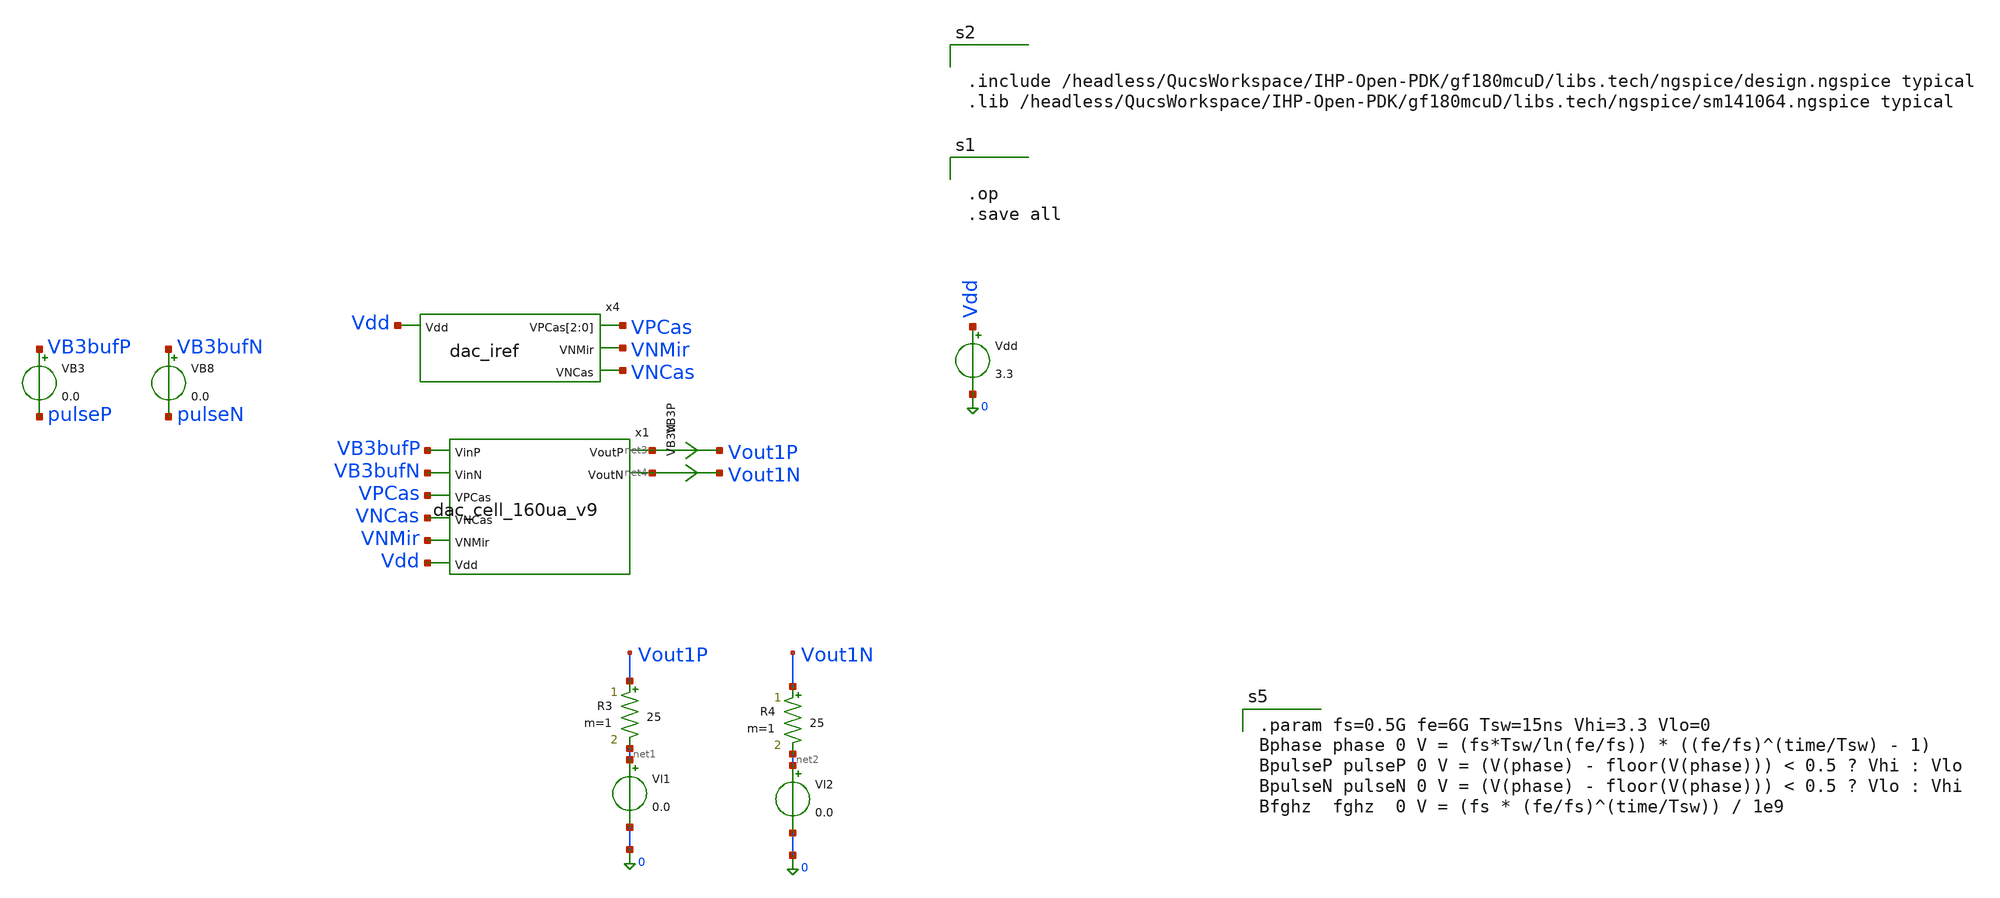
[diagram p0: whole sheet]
** sch_path: blocks/dac/test/test_dac_fsweep_160ua.sch
**.subckt test_dac_fsweep_160ua
Vdd Vdd 0 3.3
.save i(vdd)
R3 Vout1P net1 25 m=1
R4 Vout1N net2 25 m=1
Vl1 net1 0 0.0
.save i(vl1)
Vl2 net2 0 0.0
.save i(vl2)
VB3 VB3bufP pulseP 0.0
.save i(vb3)
VB8 VB3bufN pulseN 0.0
.save i(vb8)
x4 Vdd VPCas VPCas VPCas VNMir VNCas dac_iref
VB3P net3 Vout1P 0
.save i(vb3p)
VB3N net4 Vout1N 0
.save i(vb3n)
x1 net3 VB3bufP net4 VB3bufN VPCas VNCas VNMir Vdd dac_cell_160ua_v9
**** begin user architecture code



.save all
.control

tran 1p 5ns
* plot VU1syncP+6 VU1syncN+6 VU2syncP+6 VU2syncN+6 VgN+12 VgP Dm ClkP+18 ClkN+18 i(Vl1)*5E4-6
*+ i(Vl2)*5E4-6 (i(Vl1)-i(Vl2))*5E4-12
* plot ClkP+6 ClkN+6 VU0in VB1in VU0syncP-6 VU0syncN-12 VB1syncP-6 VB1syncN-12
* plot Vout1P+15E-3 Vout1N+15E-3 Vout1P-Vout1N
* plot ClkP+5 ClkN+5 VB3syncP VB3syncN VB3bufP-5 VB3bufN-5 xb3.x1.Vg1P-10 xb3.x1.Vg1N-10
plot 3.3-xb3.x1.Vg1P 3.3-xb3.x1.Vg1N

* plot x1.x1.Vcx x1.x1.Vg1P x1.x1.Vg1N

* plot VB1syncP VB1syncN-6 VB4syncN-6 VU0bufP-12 VB1bufP-12 VB4bufP-12 VU0bufN-18 VB1bufN-18
*+ VB4bufN-18
plot i(Vl1)-i(Vl2) i(Vl1)+100E-6 i(Vl2)+100E-6

let imax = 160E-6
let imin = -160E-6
plot i(VB3P)-i(VB3N) imax imin

let diff = i(Vl1)-i(Vl2)
plot pulseP diff/{imax}*5 fghz
* plot pulseP fghz

* plot i(VoutB3P)+100E-6 i(VoutB3N)+100E-6 i(VoutB3P)-i(VoutB3N) i(VoutB3N)+i(VoutB3P)
*+ i(v.x1.Vcrr1)-200E-6 i(v.x1.Vcrr2)-200E-6
* plot i(v.x1.Vcrr1) i(v.x1.Vcrr2)
* plot i(Vl1) VB1in/5E4+200E-6 VU0in/5E4+200E-6
* wrdata /foss/designs/dds/dac_isource_unary_pmos_80ua_v4_tt_500ps.csv ClkP ClkN Din VdsyncP VdsyncN
*+ i(Vl1) i(Vl2)
.endc





.op
.save all




.include /headless/QucsWorkspace/IHP-Open-PDK/gf180mcuD/libs.tech/ngspice/design.ngspice typical
.lib /headless/QucsWorkspace/IHP-Open-PDK/gf180mcuD/libs.tech/ngspice/sm141064.ngspice typical



.param fs=0.5G fe=6G Tsw=15ns Vhi=3.3 Vlo=0
Bphase phase 0 V = (fs*Tsw/ln(fe/fs)) * ((fe/fs)^(time/Tsw) - 1)
BpulseP pulseP 0 V = (V(phase) - floor(V(phase))) < 0.5 ? Vhi : Vlo
BpulseN pulseN 0 V = (V(phase) - floor(V(phase))) < 0.5 ? Vlo : Vhi
Bfghz  fghz  0 V = (fs * (fe/fs)^(time/Tsw)) / 1e9



**** end user architecture code
**.ends

* expanding   symbol:  iref/dac_iref.sym # of pins=4
** sym_path: blocks/dac/iref/dac_iref.sym
** sch_path: blocks/dac/iref/dac_iref.sch
.subckt dac_iref Vdd VPCas[2] VPCas[1] VPCas[0] VNMir VNCas
*.ipin Vdd
*.opin VPCas[2],VPCas[1],VPCas[0]
*.opin VNMir
*.opin VNCas
XM69 net3 net2 0 0 nfet_03v3 L=2u W=6u nf=1 ad='int((nf+1)/2) * W/nf * 0.18u' as='int((nf+2)/2) * W/nf * 0.18u'
+ pd='2*int((nf+1)/2) * (W/nf + 0.18u)' ps='2*int((nf+2)/2) * (W/nf + 0.18u)' nrd='0.18u / W' nrs='0.18u / W'
+ sa=0 sb=0 sd=0 m=1
XM70 net2 net1 0 0 nfet_03v3 L=2u W=4u nf=1 ad='int((nf+1)/2) * W/nf * 0.18u' as='int((nf+2)/2) * W/nf * 0.18u'
+ pd='2*int((nf+1)/2) * (W/nf + 0.18u)' ps='2*int((nf+2)/2) * (W/nf + 0.18u)' nrd='0.18u / W' nrs='0.18u / W'
+ sa=0 sb=0 sd=0 m=1
XM71 net1 net4 Vdd Vdd pfet_03v3 L=2u W=6u nf=1 ad='int((nf+1)/2) * W/nf * 0.18u' as='int((nf+2)/2) * W/nf * 0.18u'
+ pd='2*int((nf+1)/2) * (W/nf + 0.18u)' ps='2*int((nf+2)/2) * (W/nf + 0.18u)' nrd='0.18u / W' nrs='0.18u / W'
+ sa=0 sb=0 sd=0 m=1
XM72 net4 net3 Vdd Vdd pfet_03v3 L=2u W=5u nf=1 ad='int((nf+1)/2) * W/nf * 0.18u' as='int((nf+2)/2) * W/nf * 0.18u'
+ pd='2*int((nf+1)/2) * (W/nf + 0.18u)' ps='2*int((nf+2)/2) * (W/nf + 0.18u)' nrd='0.18u / W' nrs='0.18u / W'
+ sa=0 sb=0 sd=0 m=1
x1[2] Vdd VPCas[2] net4 VPCas[2] Vbias ota5t
x1[1] Vdd VPCas[1] net4 VPCas[1] Vbias ota5t
x1[0] Vdd VPCas[0] net4 VPCas[0] Vbias ota5t
XC7 net4 0 cap_mim_2f0_m3m4_noshield c_width=25e-6 c_length=20e-6 m=1
XC2[2] VPCas[2] 0 cap_mim_2f0_m3m4_noshield c_width=10e-6 c_length=5e-6 m=1
XC2[1] VPCas[1] 0 cap_mim_2f0_m3m4_noshield c_width=10e-6 c_length=5e-6 m=1
XC2[0] VPCas[0] 0 cap_mim_2f0_m3m4_noshield c_width=10e-6 c_length=5e-6 m=1
XM7 net6 net6 Vdd Vdd pfet_03v3 L=1u W=6u nf=1 ad='int((nf+1)/2) * W/nf * 0.18u' as='int((nf+2)/2) * W/nf * 0.18u'
+ pd='2*int((nf+1)/2) * (W/nf + 0.18u)' ps='2*int((nf+2)/2) * (W/nf + 0.18u)' nrd='0.18u / W' nrs='0.18u / W'
+ sa=0 sb=0 sd=0 m=1
XM8 net5 net5 net6 Vdd pfet_03v3 L=1u W=6u nf=1 ad='int((nf+1)/2) * W/nf * 0.18u' as='int((nf+2)/2) * W/nf * 0.18u'
+ pd='2*int((nf+1)/2) * (W/nf + 0.18u)' ps='2*int((nf+2)/2) * (W/nf + 0.18u)' nrd='0.18u / W' nrs='0.18u / W'
+ sa=0 sb=0 sd=0 m=1
Iref2 net5 0 DC 10uA AC 0
XM9 net7 net6 Vdd Vdd pfet_03v3 L=1u W=6u nf=1 ad='int((nf+1)/2) * W/nf * 0.18u' as='int((nf+2)/2) * W/nf * 0.18u'
+ pd='2*int((nf+1)/2) * (W/nf + 0.18u)' ps='2*int((nf+2)/2) * (W/nf + 0.18u)' nrd='0.18u / W' nrs='0.18u / W'
+ sa=0 sb=0 sd=0 m=1
XM10 VNMir net5 net7 Vdd pfet_03v3 L=1u W=6u nf=1 ad='int((nf+1)/2) * W/nf * 0.18u' as='int((nf+2)/2) * W/nf * 0.18u'
+ pd='2*int((nf+1)/2) * (W/nf + 0.18u)' ps='2*int((nf+2)/2) * (W/nf + 0.18u)' nrd='0.18u / W' nrs='0.18u / W'
+ sa=0 sb=0 sd=0 m=1
XM11 VNMir VNMir 0 0 nfet_03v3 L=4u W=2u nf=1 ad='int((nf+1)/2) * W/nf * 0.18u' as='int((nf+2)/2) * W/nf * 0.18u'
+ pd='2*int((nf+1)/2) * (W/nf + 0.18u)' ps='2*int((nf+2)/2) * (W/nf + 0.18u)' nrd='0.18u / W' nrs='0.18u / W'
+ sa=0 sb=0 sd=0 m=1
XM12 net8 net6 Vdd Vdd pfet_03v3 L=1u W=6u nf=1 ad='int((nf+1)/2) * W/nf * 0.18u' as='int((nf+2)/2) * W/nf * 0.18u'
+ pd='2*int((nf+1)/2) * (W/nf + 0.18u)' ps='2*int((nf+2)/2) * (W/nf + 0.18u)' nrd='0.18u / W' nrs='0.18u / W'
+ sa=0 sb=0 sd=0 m=1
XM14 VNCas net5 net8 Vdd pfet_03v3 L=1u W=6u nf=1 ad='int((nf+1)/2) * W/nf * 0.18u' as='int((nf+2)/2) * W/nf * 0.18u'
+ pd='2*int((nf+1)/2) * (W/nf + 0.18u)' ps='2*int((nf+2)/2) * (W/nf + 0.18u)' nrd='0.18u / W' nrs='0.18u / W'
+ sa=0 sb=0 sd=0 m=1
XM16 net9 VNCas 0 0 nfet_03v3 L=1u W=2u nf=1 ad='int((nf+1)/2) * W/nf * 0.18u' as='int((nf+2)/2) * W/nf * 0.18u'
+ pd='2*int((nf+1)/2) * (W/nf + 0.18u)' ps='2*int((nf+2)/2) * (W/nf + 0.18u)' nrd='0.18u / W' nrs='0.18u / W'
+ sa=0 sb=0 sd=0 m=1
XM17 VNCas VNMir net9 0 nfet_03v3 L=1u W=2u nf=1 ad='int((nf+1)/2) * W/nf * 0.18u' as='int((nf+2)/2) * W/nf * 0.18u'
+ pd='2*int((nf+1)/2) * (W/nf + 0.18u)' ps='2*int((nf+2)/2) * (W/nf + 0.18u)' nrd='0.18u / W' nrs='0.18u / W'
+ sa=0 sb=0 sd=0 m=1
XM4 Vbias VNMir net10 0 nfet_03v3 L=1u W=2u nf=1 ad='int((nf+1)/2) * W/nf * 0.18u' as='int((nf+2)/2) * W/nf * 0.18u'
+ pd='2*int((nf+1)/2) * (W/nf + 0.18u)' ps='2*int((nf+2)/2) * (W/nf + 0.18u)' nrd='0.18u / W' nrs='0.18u / W'
+ sa=0 sb=0 sd=0 m=1
XM5 Vbias Vbias Vdd Vdd pfet_03v3 L=1u W=4u nf=1 ad='int((nf+1)/2) * W/nf * 0.18u' as='int((nf+2)/2) * W/nf * 0.18u'
+ pd='2*int((nf+1)/2) * (W/nf + 0.18u)' ps='2*int((nf+2)/2) * (W/nf + 0.18u)' nrd='0.18u / W' nrs='0.18u / W'
+ sa=0 sb=0 sd=0 m=1
XM13 net10 VNCas 0 0 nfet_03v3 L=1u W=2u nf=1 ad='int((nf+1)/2) * W/nf * 0.18u' as='int((nf+2)/2) * W/nf * 0.18u'
+ pd='2*int((nf+1)/2) * (W/nf + 0.18u)' ps='2*int((nf+2)/2) * (W/nf + 0.18u)' nrd='0.18u / W' nrs='0.18u / W'
+ sa=0 sb=0 sd=0 m=1
XR3 net4 net3 Vdd ppolyf_u_1k r_width=1e-6 r_length=4e-6 m=1
XR2 net1 net2 Vdd ppolyf_u_1k r_width=1e-6 r_length=8e-6 m=1
.ends


* expanding   symbol:  cellv9/dac_cell_160ua_v9.sym # of pins=8
** sym_path: blocks/dac/cellv9/dac_cell_160ua_v9.sym
** sch_path: blocks/dac/cellv9/dac_cell_160ua_v9.sch
.subckt dac_cell_160ua_v9 VoutP VinP VoutN VinN VPCas VNCas VNMir Vdd
*.opin VoutP
*.opin VoutN
*.ipin VinP
*.ipin VinN
*.ipin Vdd
*.ipin VPCas
*.ipin VNCas
*.ipin VNMir
x5 VoutP VinP VoutN VinN VPCas VNCas VNMir Vdd dac_cell_80ua_v9
x2 VoutP VinP VoutN VinN VPCas VNCas VNMir Vdd dac_cell_80ua_v9
.ends


* expanding   symbol:  common/ota5t.sym # of pins=5
** sym_path: blocks/dac/common/ota5t.sym
** sch_path: blocks/dac/common/ota5t.sch
.subckt ota5t Vdd VinN VinP Vout Vbias
*.ipin VinP
*.ipin VinN
*.opin Vout
*.ipin Vdd
*.ipin Vbias
XM16 Vout net2 0 0 nfet_03v3 L=1u W=2u nf=1 ad='int((nf+1)/2) * W/nf * 0.18u' as='int((nf+2)/2) * W/nf * 0.18u'
+ pd='2*int((nf+1)/2) * (W/nf + 0.18u)' ps='2*int((nf+2)/2) * (W/nf + 0.18u)' nrd='0.18u / W' nrs='0.18u / W'
+ sa=0 sb=0 sd=0 m=1
XM1 Vout VinN net1 Vdd pfet_03v3 L=1u W=4u nf=1 ad='int((nf+1)/2) * W/nf * 0.18u' as='int((nf+2)/2) * W/nf * 0.18u'
+ pd='2*int((nf+1)/2) * (W/nf + 0.18u)' ps='2*int((nf+2)/2) * (W/nf + 0.18u)' nrd='0.18u / W' nrs='0.18u / W'
+ sa=0 sb=0 sd=0 m=1
XM19 net2 VinP net1 Vdd pfet_03v3 L=1u W=4u nf=1 ad='int((nf+1)/2) * W/nf * 0.18u' as='int((nf+2)/2) * W/nf * 0.18u'
+ pd='2*int((nf+1)/2) * (W/nf + 0.18u)' ps='2*int((nf+2)/2) * (W/nf + 0.18u)' nrd='0.18u / W' nrs='0.18u / W'
+ sa=0 sb=0 sd=0 m=1
XM22 net2 net2 0 0 nfet_03v3 L=1u W=2u nf=1 ad='int((nf+1)/2) * W/nf * 0.18u' as='int((nf+2)/2) * W/nf * 0.18u'
+ pd='2*int((nf+1)/2) * (W/nf + 0.18u)' ps='2*int((nf+2)/2) * (W/nf + 0.18u)' nrd='0.18u / W' nrs='0.18u / W'
+ sa=0 sb=0 sd=0 m=1
.param bbW=2u
.param bbL=1u
XM29 net1 Vbias Vdd Vdd pfet_03v3 L=1u W=4u nf=1 ad='int((nf+1)/2) * W/nf * 0.18u' as='int((nf+2)/2) * W/nf * 0.18u'
+ pd='2*int((nf+1)/2) * (W/nf + 0.18u)' ps='2*int((nf+2)/2) * (W/nf + 0.18u)' nrd='0.18u / W' nrs='0.18u / W'
+ sa=0 sb=0 sd=0 m=2
.ends


* expanding   symbol:  cellv9/dac_cell_80ua_v9.sym # of pins=8
** sym_path: blocks/dac/cellv9/dac_cell_80ua_v9.sym
** sch_path: blocks/dac/cellv9/dac_cell_80ua_v9.sch
.subckt dac_cell_80ua_v9 VoutP VinP VoutN VinN VPCas VNCas VNMir Vdd
*.opin VoutP
*.opin VoutN
*.ipin VinP
*.ipin VinN
*.ipin Vdd
*.ipin VPCas
*.ipin VNCas
*.ipin VNMir
.param cmLw=0.4u
.param cmHw=0.7u
.param cmLfbw=1.0u
.param cmHfbw=0.22u
XM20 VxP Vg1P Vcx Vdd pfet_03v3 L=0.28u W={cswW} nf=1 ad='int((nf+1)/2) * W/nf * 0.18u' as='int((nf+2)/2) * W/nf * 0.18u'
+ pd='2*int((nf+1)/2) * (W/nf + 0.18u)' ps='2*int((nf+2)/2) * (W/nf + 0.18u)' nrd='0.18u / W' nrs='0.18u / W'
+ sa=0 sb=0 sd=0 m=1
XM21 VxN Vg1N Vcx Vdd pfet_03v3 L=0.28u W={cswW} nf=1 ad='int((nf+1)/2) * W/nf * 0.18u' as='int((nf+2)/2) * W/nf * 0.18u'
+ pd='2*int((nf+1)/2) * (W/nf + 0.18u)' ps='2*int((nf+2)/2) * (W/nf + 0.18u)' nrd='0.18u / W' nrs='0.18u / W'
+ sa=0 sb=0 sd=0 m=1
XM22 VoutP VcbP VxP Vdd pfet_03v3 L=0.28u W={cbufW} nf=1 ad='int((nf+1)/2) * W/nf * 0.18u' as='int((nf+2)/2) * W/nf * 0.18u'
+ pd='2*int((nf+1)/2) * (W/nf + 0.18u)' ps='2*int((nf+2)/2) * (W/nf + 0.18u)' nrd='0.18u / W' nrs='0.18u / W'
+ sa=0 sb=0 sd=0 m=1
XM23 VoutN VcbN VxN Vdd pfet_03v3 L=0.28u W={cbufW} nf=1 ad='int((nf+1)/2) * W/nf * 0.18u' as='int((nf+2)/2) * W/nf * 0.18u'
+ pd='2*int((nf+1)/2) * (W/nf + 0.18u)' ps='2*int((nf+2)/2) * (W/nf + 0.18u)' nrd='0.18u / W' nrs='0.18u / W'
+ sa=0 sb=0 sd=0 m=1
XM24 net1 Vg1N Vdd Vdd pfet_03v3 L=0.28u W={invPw} nf=1 ad='int((nf+1)/2) * W/nf * 0.18u' as='int((nf+2)/2) * W/nf * 0.18u'
+ pd='2*int((nf+1)/2) * (W/nf + 0.18u)' ps='2*int((nf+2)/2) * (W/nf + 0.18u)' nrd='0.18u / W' nrs='0.18u / W'
+ sa=0 sb=0 sd=0 m=1
XM34 net1 Vg1N 0 0 nfet_03v3 L=0.28u W=0.22u nf=1 ad='int((nf+1)/2) * W/nf * 0.18u' as='int((nf+2)/2) * W/nf * 0.18u'
+ pd='2*int((nf+1)/2) * (W/nf + 0.18u)' ps='2*int((nf+2)/2) * (W/nf + 0.18u)' nrd='0.18u / W' nrs='0.18u / W'
+ sa=0 sb=0 sd=0 m=1
XM35 VoutN net1 VoutN Vdd pfet_03v3 L=0.28u W={dummyW} nf=1 ad='int((nf+1)/2) * W/nf * 0.18u' as='int((nf+2)/2) * W/nf * 0.18u'
+ pd='2*int((nf+1)/2) * (W/nf + 0.18u)' ps='2*int((nf+2)/2) * (W/nf + 0.18u)' nrd='0.18u / W' nrs='0.18u / W'
+ sa=0 sb=0 sd=0 m=1
XM36 net2 Vg1P Vdd Vdd pfet_03v3 L=0.28u W={invPw} nf=1 ad='int((nf+1)/2) * W/nf * 0.18u' as='int((nf+2)/2) * W/nf * 0.18u'
+ pd='2*int((nf+1)/2) * (W/nf + 0.18u)' ps='2*int((nf+2)/2) * (W/nf + 0.18u)' nrd='0.18u / W' nrs='0.18u / W'
+ sa=0 sb=0 sd=0 m=1
XM37 net2 Vg1P 0 0 nfet_03v3 L=0.28u W=0.22u nf=1 ad='int((nf+1)/2) * W/nf * 0.18u' as='int((nf+2)/2) * W/nf * 0.18u'
+ pd='2*int((nf+1)/2) * (W/nf + 0.18u)' ps='2*int((nf+2)/2) * (W/nf + 0.18u)' nrd='0.18u / W' nrs='0.18u / W'
+ sa=0 sb=0 sd=0 m=1
XM38 VoutP net2 VoutP Vdd pfet_03v3 L=0.28u W={dummyW} nf=1 ad='int((nf+1)/2) * W/nf * 0.18u' as='int((nf+2)/2) * W/nf * 0.18u'
+ pd='2*int((nf+1)/2) * (W/nf + 0.18u)' ps='2*int((nf+2)/2) * (W/nf + 0.18u)' nrd='0.18u / W' nrs='0.18u / W'
+ sa=0 sb=0 sd=0 m=1
VcbRef3 VcbRef 0 {Vcbias}
.save i(vcbref3)
.param VcBias=0.84
.param casW=4u
XM39 net3 VinPDr VH Vdd pfet_03v3 L=0.28u W={cmHw} nf=1 ad='int((nf+1)/2) * W/nf * 0.18u' as='int((nf+2)/2) * W/nf * 0.18u'
+ pd='2*int((nf+1)/2) * (W/nf + 0.18u)' ps='2*int((nf+2)/2) * (W/nf + 0.18u)' nrd='0.18u / W' nrs='0.18u / W'
+ sa=0 sb=0 sd=0 m=1
XM40 Vg1P VinPDr net3 Vdd pfet_03v3 L=0.28u W={cmHw} nf=1 ad='int((nf+1)/2) * W/nf * 0.18u' as='int((nf+2)/2) * W/nf * 0.18u'
+ pd='2*int((nf+1)/2) * (W/nf + 0.18u)' ps='2*int((nf+2)/2) * (W/nf + 0.18u)' nrd='0.18u / W' nrs='0.18u / W'
+ sa=0 sb=0 sd=0 m=1
XM41 Vg1P VinPDr VL 0 nfet_03v3 L=0.28u W={cmLw} nf=1 ad='int((nf+1)/2) * W/nf * 0.18u' as='int((nf+2)/2) * W/nf * 0.18u'
+ pd='2*int((nf+1)/2) * (W/nf + 0.18u)' ps='2*int((nf+2)/2) * (W/nf + 0.18u)' nrd='0.18u / W' nrs='0.18u / W'
+ sa=0 sb=0 sd=0 m=1
XM42 net3 VinNDr VH Vdd pfet_03v3 L=0.28u W={cmHfbW} nf=1 ad='int((nf+1)/2) * W/nf * 0.18u' as='int((nf+2)/2) * W/nf * 0.18u'
+ pd='2*int((nf+1)/2) * (W/nf + 0.18u)' ps='2*int((nf+2)/2) * (W/nf + 0.18u)' nrd='0.18u / W' nrs='0.18u / W'
+ sa=0 sb=0 sd=0 m=1
XM43 net4 VinNDr VH Vdd pfet_03v3 L=0.28u W={cmHw} nf=1 ad='int((nf+1)/2) * W/nf * 0.18u' as='int((nf+2)/2) * W/nf * 0.18u'
+ pd='2*int((nf+1)/2) * (W/nf + 0.18u)' ps='2*int((nf+2)/2) * (W/nf + 0.18u)' nrd='0.18u / W' nrs='0.18u / W'
+ sa=0 sb=0 sd=0 m=1
XM44 Vg1N VinNDr net4 Vdd pfet_03v3 L=0.28u W={cmHw} nf=1 ad='int((nf+1)/2) * W/nf * 0.18u' as='int((nf+2)/2) * W/nf * 0.18u'
+ pd='2*int((nf+1)/2) * (W/nf + 0.18u)' ps='2*int((nf+2)/2) * (W/nf + 0.18u)' nrd='0.18u / W' nrs='0.18u / W'
+ sa=0 sb=0 sd=0 m=1
XM45 Vg1N VinNDr VL 0 nfet_03v3 L=0.28u W={cmLw} nf=1 ad='int((nf+1)/2) * W/nf * 0.18u' as='int((nf+2)/2) * W/nf * 0.18u'
+ pd='2*int((nf+1)/2) * (W/nf + 0.18u)' ps='2*int((nf+2)/2) * (W/nf + 0.18u)' nrd='0.18u / W' nrs='0.18u / W'
+ sa=0 sb=0 sd=0 m=1
XM46 net4 VinPDr VH Vdd pfet_03v3 L=0.28u W={cmHfbW} nf=1 ad='int((nf+1)/2) * W/nf * 0.18u' as='int((nf+2)/2) * W/nf * 0.18u'
+ pd='2*int((nf+1)/2) * (W/nf + 0.18u)' ps='2*int((nf+2)/2) * (W/nf + 0.18u)' nrd='0.18u / W' nrs='0.18u / W'
+ sa=0 sb=0 sd=0 m=1
XM47 VL VinPDr Vg1N Vdd pfet_03v3 L=0.28u W={cmLfbw} nf=1 ad='int((nf+1)/2) * W/nf * 0.18u' as='int((nf+2)/2) * W/nf * 0.18u'
+ pd='2*int((nf+1)/2) * (W/nf + 0.18u)' ps='2*int((nf+2)/2) * (W/nf + 0.18u)' nrd='0.18u / W' nrs='0.18u / W'
+ sa=0 sb=0 sd=0 m=1
XM48 VL VinNDr Vg1P Vdd pfet_03v3 L=0.28u W={cmLfbw} nf=1 ad='int((nf+1)/2) * W/nf * 0.18u' as='int((nf+2)/2) * W/nf * 0.18u'
+ pd='2*int((nf+1)/2) * (W/nf + 0.18u)' ps='2*int((nf+2)/2) * (W/nf + 0.18u)' nrd='0.18u / W' nrs='0.18u / W'
+ sa=0 sb=0 sd=0 m=1
.param dummyW=1.0u
.param invPW=0.5u
.param cswW=3.0u
.param cbufW=3.2u
x1 VH Vdd VL clamp
.param mirW=4u
.param mirL=1u
.param casL=1u
XM4 net5 VPCas Vdd Vdd pfet_03v3 L={casL} W={casW} nf=1 ad='int((nf+1)/2) * W/nf * 0.18u' as='int((nf+2)/2) * W/nf * 0.18u'
+ pd='2*int((nf+1)/2) * (W/nf + 0.18u)' ps='2*int((nf+2)/2) * (W/nf + 0.18u)' nrd='0.18u / W' nrs='0.18u / W'
+ sa=0 sb=0 sd=0 m=1
XM7 Vcx VPMir net5 Vdd pfet_03v3 L={mirL} W={mirW} nf=1 ad='int((nf+1)/2) * W/nf * 0.18u' as='int((nf+2)/2) * W/nf * 0.18u'
+ pd='2*int((nf+1)/2) * (W/nf + 0.18u)' ps='2*int((nf+2)/2) * (W/nf + 0.18u)' nrd='0.18u / W' nrs='0.18u / W'
+ sa=0 sb=0 sd=0 m=1
XM9 net6 VPCas Vdd Vdd pfet_03v3 L={casL} W={casW} nf=1 ad='int((nf+1)/2) * W/nf * 0.18u' as='int((nf+2)/2) * W/nf * 0.18u'
+ pd='2*int((nf+1)/2) * (W/nf + 0.18u)' ps='2*int((nf+2)/2) * (W/nf + 0.18u)' nrd='0.18u / W' nrs='0.18u / W'
+ sa=0 sb=0 sd=0 m=1
XM10 Vcx VPMir net6 Vdd pfet_03v3 L={mirL} W={mirW} nf=1 ad='int((nf+1)/2) * W/nf * 0.18u' as='int((nf+2)/2) * W/nf * 0.18u'
+ pd='2*int((nf+1)/2) * (W/nf + 0.18u)' ps='2*int((nf+2)/2) * (W/nf + 0.18u)' nrd='0.18u / W' nrs='0.18u / W'
+ sa=0 sb=0 sd=0 m=1
XM11 net7 VPCas Vdd Vdd pfet_03v3 L={casL} W={casW} nf=1 ad='int((nf+1)/2) * W/nf * 0.18u' as='int((nf+2)/2) * W/nf * 0.18u'
+ pd='2*int((nf+1)/2) * (W/nf + 0.18u)' ps='2*int((nf+2)/2) * (W/nf + 0.18u)' nrd='0.18u / W' nrs='0.18u / W'
+ sa=0 sb=0 sd=0 m=1
XM12 Vcx VPMir net7 Vdd pfet_03v3 L={mirL} W={mirW} nf=1 ad='int((nf+1)/2) * W/nf * 0.18u' as='int((nf+2)/2) * W/nf * 0.18u'
+ pd='2*int((nf+1)/2) * (W/nf + 0.18u)' ps='2*int((nf+2)/2) * (W/nf + 0.18u)' nrd='0.18u / W' nrs='0.18u / W'
+ sa=0 sb=0 sd=0 m=1
XM13 net8 VPCas Vdd Vdd pfet_03v3 L={casL} W={casW} nf=1 ad='int((nf+1)/2) * W/nf * 0.18u' as='int((nf+2)/2) * W/nf * 0.18u'
+ pd='2*int((nf+1)/2) * (W/nf + 0.18u)' ps='2*int((nf+2)/2) * (W/nf + 0.18u)' nrd='0.18u / W' nrs='0.18u / W'
+ sa=0 sb=0 sd=0 m=1
XM14 Vcx VPMir net8 Vdd pfet_03v3 L={mirL} W={mirW} nf=1 ad='int((nf+1)/2) * W/nf * 0.18u' as='int((nf+2)/2) * W/nf * 0.18u'
+ pd='2*int((nf+1)/2) * (W/nf + 0.18u)' ps='2*int((nf+2)/2) * (W/nf + 0.18u)' nrd='0.18u / W' nrs='0.18u / W'
+ sa=0 sb=0 sd=0 m=1
XM1 net9 VPCas Vdd Vdd pfet_03v3 L={casL} W={casW} nf=1 ad='int((nf+1)/2) * W/nf * 0.18u' as='int((nf+2)/2) * W/nf * 0.18u'
+ pd='2*int((nf+1)/2) * (W/nf + 0.18u)' ps='2*int((nf+2)/2) * (W/nf + 0.18u)' nrd='0.18u / W' nrs='0.18u / W'
+ sa=0 sb=0 sd=0 m=1
XM5 Vcx VPMir net9 Vdd pfet_03v3 L={mirL} W={mirW} nf=1 ad='int((nf+1)/2) * W/nf * 0.18u' as='int((nf+2)/2) * W/nf * 0.18u'
+ pd='2*int((nf+1)/2) * (W/nf + 0.18u)' ps='2*int((nf+2)/2) * (W/nf + 0.18u)' nrd='0.18u / W' nrs='0.18u / W'
+ sa=0 sb=0 sd=0 m=1
XM6 net10 VPCas Vdd Vdd pfet_03v3 L={casL} W={casW} nf=1 ad='int((nf+1)/2) * W/nf * 0.18u' as='int((nf+2)/2) * W/nf * 0.18u'
+ pd='2*int((nf+1)/2) * (W/nf + 0.18u)' ps='2*int((nf+2)/2) * (W/nf + 0.18u)' nrd='0.18u / W' nrs='0.18u / W'
+ sa=0 sb=0 sd=0 m=1
XM8 Vcx VPMir net10 Vdd pfet_03v3 L={mirL} W={mirW} nf=1 ad='int((nf+1)/2) * W/nf * 0.18u' as='int((nf+2)/2) * W/nf * 0.18u'
+ pd='2*int((nf+1)/2) * (W/nf + 0.18u)' ps='2*int((nf+2)/2) * (W/nf + 0.18u)' nrd='0.18u / W' nrs='0.18u / W'
+ sa=0 sb=0 sd=0 m=1
XM15 net11 VPCas Vdd Vdd pfet_03v3 L={casL} W={casW} nf=1 ad='int((nf+1)/2) * W/nf * 0.18u' as='int((nf+2)/2) * W/nf * 0.18u'
+ pd='2*int((nf+1)/2) * (W/nf + 0.18u)' ps='2*int((nf+2)/2) * (W/nf + 0.18u)' nrd='0.18u / W' nrs='0.18u / W'
+ sa=0 sb=0 sd=0 m=1
XM16 Vcx VPMir net11 Vdd pfet_03v3 L={mirL} W={mirW} nf=1 ad='int((nf+1)/2) * W/nf * 0.18u' as='int((nf+2)/2) * W/nf * 0.18u'
+ pd='2*int((nf+1)/2) * (W/nf + 0.18u)' ps='2*int((nf+2)/2) * (W/nf + 0.18u)' nrd='0.18u / W' nrs='0.18u / W'
+ sa=0 sb=0 sd=0 m=1
XM17 net12 VPCas Vdd Vdd pfet_03v3 L={casL} W={casW} nf=1 ad='int((nf+1)/2) * W/nf * 0.18u' as='int((nf+2)/2) * W/nf * 0.18u'
+ pd='2*int((nf+1)/2) * (W/nf + 0.18u)' ps='2*int((nf+2)/2) * (W/nf + 0.18u)' nrd='0.18u / W' nrs='0.18u / W'
+ sa=0 sb=0 sd=0 m=1
XM18 Vcx VPMir net12 Vdd pfet_03v3 L={mirL} W={mirW} nf=1 ad='int((nf+1)/2) * W/nf * 0.18u' as='int((nf+2)/2) * W/nf * 0.18u'
+ pd='2*int((nf+1)/2) * (W/nf + 0.18u)' ps='2*int((nf+2)/2) * (W/nf + 0.18u)' nrd='0.18u / W' nrs='0.18u / W'
+ sa=0 sb=0 sd=0 m=1
XM2 VPMir VNMir net13 0 nfet_03v3 L=1u W=2u nf=1 ad='int((nf+1)/2) * W/nf * 0.18u' as='int((nf+2)/2) * W/nf * 0.18u'
+ pd='2*int((nf+1)/2) * (W/nf + 0.18u)' ps='2*int((nf+2)/2) * (W/nf + 0.18u)' nrd='0.18u / W' nrs='0.18u / W'
+ sa=0 sb=0 sd=0 m=1
XM3 VPMir VPMir net14 Vdd pfet_03v3 L={mirL} W={mirW} nf=1 ad='int((nf+1)/2) * W/nf * 0.18u' as='int((nf+2)/2) * W/nf * 0.18u'
+ pd='2*int((nf+1)/2) * (W/nf + 0.18u)' ps='2*int((nf+2)/2) * (W/nf + 0.18u)' nrd='0.18u / W' nrs='0.18u / W'
+ sa=0 sb=0 sd=0 m=1
XM19 net13 VNCas 0 0 nfet_03v3 L=1u W=2u nf=1 ad='int((nf+1)/2) * W/nf * 0.18u' as='int((nf+2)/2) * W/nf * 0.18u'
+ pd='2*int((nf+1)/2) * (W/nf + 0.18u)' ps='2*int((nf+2)/2) * (W/nf + 0.18u)' nrd='0.18u / W' nrs='0.18u / W'
+ sa=0 sb=0 sd=0 m=1
XM25 net14 VPCas Vdd Vdd pfet_03v3 L={casL} W={casW} nf=1 ad='int((nf+1)/2) * W/nf * 0.18u' as='int((nf+2)/2) * W/nf * 0.18u'
+ pd='2*int((nf+1)/2) * (W/nf + 0.18u)' ps='2*int((nf+2)/2) * (W/nf + 0.18u)' nrd='0.18u / W' nrs='0.18u / W'
+ sa=0 sb=0 sd=0 m=1
x2 Vdd VcbP VcbRef VcbP IB10 ota5_ab_buf_v1
x3 Vdd VcbN VcbRef VcbN IB10 ota5_ab_buf_v1
VinN net17 net18 0
.save i(vinn)
x5 net17 VinN Vdd cmos_buf
VinP net19 net20 0
.save i(vinp)
x4 net19 VinP Vdd cmos_buf
XM26 net15 VNMir net16 0 nfet_03v3 L=1u W=2u nf=1 ad='int((nf+1)/2) * W/nf * 0.18u' as='int((nf+2)/2) * W/nf * 0.18u'
+ pd='2*int((nf+1)/2) * (W/nf + 0.18u)' ps='2*int((nf+2)/2) * (W/nf + 0.18u)' nrd='0.18u / W' nrs='0.18u / W'
+ sa=0 sb=0 sd=0 m=1
XM27 net16 VNCas 0 0 nfet_03v3 L=1u W=2u nf=1 ad='int((nf+1)/2) * W/nf * 0.18u' as='int((nf+2)/2) * W/nf * 0.18u'
+ pd='2*int((nf+1)/2) * (W/nf + 0.18u)' ps='2*int((nf+2)/2) * (W/nf + 0.18u)' nrd='0.18u / W' nrs='0.18u / W'
+ sa=0 sb=0 sd=0 m=1
XM28 net15 net15 Vdd Vdd pfet_03v3 L=1u W=8u nf=1 ad='int((nf+1)/2) * W/nf * 0.18u' as='int((nf+2)/2) * W/nf * 0.18u'
+ pd='2*int((nf+1)/2) * (W/nf + 0.18u)' ps='2*int((nf+2)/2) * (W/nf + 0.18u)' nrd='0.18u / W' nrs='0.18u / W'
+ sa=0 sb=0 sd=0 m=1
XM29 IB10 net15 Vdd Vdd pfet_03v3 L=1u W=8u nf=1 ad='int((nf+1)/2) * W/nf * 0.18u' as='int((nf+2)/2) * W/nf * 0.18u'
+ pd='2*int((nf+1)/2) * (W/nf + 0.18u)' ps='2*int((nf+2)/2) * (W/nf + 0.18u)' nrd='0.18u / W' nrs='0.18u / W'
+ sa=0 sb=0 sd=0 m=1
XM30 IB10 IB10 0 0 nfet_03v3 L=1u W=8u nf=1 ad='int((nf+1)/2) * W/nf * 0.18u' as='int((nf+2)/2) * W/nf * 0.18u'
+ pd='2*int((nf+1)/2) * (W/nf + 0.18u)' ps='2*int((nf+2)/2) * (W/nf + 0.18u)' nrd='0.18u / W' nrs='0.18u / W'
+ sa=0 sb=0 sd=0 m=1
XR3 net18 VinNDr Vdd ppolyf_u_1k r_width=1e-6 r_length=1e-6 m=1
XR2 VinPDr net20 Vdd ppolyf_u_1k r_width=1e-6 r_length=1e-6 m=1
XC4 VPMir 0 cap_mim_2f0_m3m4_noshield c_width=25e-6 c_length=20e-6 m=1
XC2 IB10 0 cap_mim_2f0_m3m4_noshield c_width=25e-6 c_length=20e-6 m=1
XC7 Vdd 0 cap_mim_2f0_m3m4_noshield c_width=25e-6 c_length=20e-6 m=1
.ends


* expanding   symbol:  cellv9/clamp.sym # of pins=3
** sym_path: blocks/dac/cellv9/clamp.sym
** sch_path: blocks/dac/cellv9/clamp.sch
.subckt clamp VH Vdd VL
*.opin VH
*.opin VL
*.ipin Vdd
XM49 VL FB 0 0 nfet_03v3 L=0.28u W=2u nf=1 ad='int((nf+1)/2) * W/nf * 0.18u' as='int((nf+2)/2) * W/nf * 0.18u'
+ pd='2*int((nf+1)/2) * (W/nf + 0.18u)' ps='2*int((nf+2)/2) * (W/nf + 0.18u)' nrd='0.18u / W' nrs='0.18u / W'
+ sa=0 sb=0 sd=0 m=1
XM50 VH FB Vdd Vdd pfet_03v3 L=0.28u W=4u nf=1 ad='int((nf+1)/2) * W/nf * 0.18u' as='int((nf+2)/2) * W/nf * 0.18u'
+ pd='2*int((nf+1)/2) * (W/nf + 0.18u)' ps='2*int((nf+2)/2) * (W/nf + 0.18u)' nrd='0.18u / W' nrs='0.18u / W'
+ sa=0 sb=0 sd=0 m=1
XR3 VL FB Vdd ppolyf_u_1k r_width=1e-6 r_length=1e-6 m=1
XR1 FB VH Vdd ppolyf_u_1k r_width=1e-6 r_length=15e-6 m=1
XC2 Vdd VH cap_mim_2f0_m3m4_noshield c_width=25e-6 c_length=20e-6 m=1
XC1 Vdd VH cap_mim_2f0_m3m4_noshield c_width=10e-6 c_length=5e-6 m=1
XC3 Vdd VH cap_mim_2f0_m3m4_noshield c_width=5e-6 c_length=5e-6 m=1
XC4 VL 0 cap_mim_2f0_m3m4_noshield c_width=25e-6 c_length=20e-6 m=1
XC5 VL 0 cap_mim_2f0_m3m4_noshield c_width=10e-6 c_length=5e-6 m=1
XC6 VL 0 cap_mim_2f0_m3m4_noshield c_width=5e-6 c_length=5e-6 m=1
XC7 Vdd 0 cap_mim_2f0_m3m4_noshield c_width=25e-6 c_length=20e-6 m=1
.ends


* expanding   symbol:  cellv9/ota5_ab_buf_v1.sym # of pins=5
** sym_path: blocks/dac/cellv9/ota5_ab_buf_v1.sym
** sch_path: blocks/dac/cellv9/ota5_ab_buf_v1.sch
.subckt ota5_ab_buf_v1 Vdd VinN VinP Vout IB10
*.opin Vout
*.ipin VinP
*.ipin VinN
*.ipin Vdd
*.ipin IB10
XM16 VoOTA net2 0 0 nfet_03v3 L=1u W=10u nf=1 ad='int((nf+1)/2) * W/nf * 0.18u' as='int((nf+2)/2) * W/nf * 0.18u'
+ pd='2*int((nf+1)/2) * (W/nf + 0.18u)' ps='2*int((nf+2)/2) * (W/nf + 0.18u)' nrd='0.18u / W' nrs='0.18u / W'
+ sa=0 sb=0 sd=0 m=1
XM18 VoOTA VinN net1 Vdd pfet_03v3 L=1u W=20u nf=1 ad='int((nf+1)/2) * W/nf * 0.18u' as='int((nf+2)/2) * W/nf * 0.18u'
+ pd='2*int((nf+1)/2) * (W/nf + 0.18u)' ps='2*int((nf+2)/2) * (W/nf + 0.18u)' nrd='0.18u / W' nrs='0.18u / W'
+ sa=0 sb=0 sd=0 m=1
XM19 net2 VinP net1 Vdd pfet_03v3 L=1u W=20u nf=1 ad='int((nf+1)/2) * W/nf * 0.18u' as='int((nf+2)/2) * W/nf * 0.18u'
+ pd='2*int((nf+1)/2) * (W/nf + 0.18u)' ps='2*int((nf+2)/2) * (W/nf + 0.18u)' nrd='0.18u / W' nrs='0.18u / W'
+ sa=0 sb=0 sd=0 m=1
XM22 net2 net2 0 0 nfet_03v3 L=1u W=10u nf=1 ad='int((nf+1)/2) * W/nf * 0.18u' as='int((nf+2)/2) * W/nf * 0.18u'
+ pd='2*int((nf+1)/2) * (W/nf + 0.18u)' ps='2*int((nf+2)/2) * (W/nf + 0.18u)' nrd='0.18u / W' nrs='0.18u / W'
+ sa=0 sb=0 sd=0 m=1
XM1 net1 net3 Vdd Vdd pfet_03v3 L=1u W=40u nf=1 ad='int((nf+1)/2) * W/nf * 0.18u' as='int((nf+2)/2) * W/nf * 0.18u'
+ pd='2*int((nf+1)/2) * (W/nf + 0.18u)' ps='2*int((nf+2)/2) * (W/nf + 0.18u)' nrd='0.18u / W' nrs='0.18u / W'
+ sa=0 sb=0 sd=0 m=1
XM2 net3 net3 Vdd Vdd pfet_03v3 L=1u W=40u nf=1 ad='int((nf+1)/2) * W/nf * 0.18u' as='int((nf+2)/2) * W/nf * 0.18u'
+ pd='2*int((nf+1)/2) * (W/nf + 0.18u)' ps='2*int((nf+2)/2) * (W/nf + 0.18u)' nrd='0.18u / W' nrs='0.18u / W'
+ sa=0 sb=0 sd=0 m=1
XM3 VI1b VI1a VI2 Vdd pfet_03v3 L=0.5u W=40u nf=1 ad='int((nf+1)/2) * W/nf * 0.18u' as='int((nf+2)/2) * W/nf * 0.18u'
+ pd='2*int((nf+1)/2) * (W/nf + 0.18u)' ps='2*int((nf+2)/2) * (W/nf + 0.18u)' nrd='0.18u / W' nrs='0.18u / W'
+ sa=0 sb=0 sd=0 m=1
XM4 VI2 VoOTA Vout 0 nfet_03v3 L=0.5u W=80u nf=1 ad='int((nf+1)/2) * W/nf * 0.18u' as='int((nf+2)/2) * W/nf * 0.18u'
+ pd='2*int((nf+1)/2) * (W/nf + 0.18u)' ps='2*int((nf+2)/2) * (W/nf + 0.18u)' nrd='0.18u / W' nrs='0.18u / W'
+ sa=0 sb=0 sd=0 m=1
XM5 Vout VI2 Vdd Vdd pfet_03v3 L=1u W=80u nf=1 ad='int((nf+1)/2) * W/nf * 0.18u' as='int((nf+2)/2) * W/nf * 0.18u'
+ pd='2*int((nf+1)/2) * (W/nf + 0.18u)' ps='2*int((nf+2)/2) * (W/nf + 0.18u)' nrd='0.18u / W' nrs='0.18u / W'
+ sa=0 sb=0 sd=0 m=1
XM6 Vout VI1b 0 0 nfet_03v3 L=0.5u W=40u nf=1 ad='int((nf+1)/2) * W/nf * 0.18u' as='int((nf+2)/2) * W/nf * 0.18u'
+ pd='2*int((nf+1)/2) * (W/nf + 0.18u)' ps='2*int((nf+2)/2) * (W/nf + 0.18u)' nrd='0.18u / W' nrs='0.18u / W'
+ sa=0 sb=0 sd=0 m=1
XM7 VI1a VI1a VI0 Vdd pfet_03v3 L=0.5u W=40u nf=1 ad='int((nf+1)/2) * W/nf * 0.18u' as='int((nf+2)/2) * W/nf * 0.18u'
+ pd='2*int((nf+1)/2) * (W/nf + 0.18u)' ps='2*int((nf+2)/2) * (W/nf + 0.18u)' nrd='0.18u / W' nrs='0.18u / W'
+ sa=0 sb=0 sd=0 m=1
XM8 VI1a VI0 Vdd Vdd pfet_03v3 L=1u W=80u nf=1 ad='int((nf+1)/2) * W/nf * 0.18u' as='int((nf+2)/2) * W/nf * 0.18u'
+ pd='2*int((nf+1)/2) * (W/nf + 0.18u)' ps='2*int((nf+2)/2) * (W/nf + 0.18u)' nrd='0.18u / W' nrs='0.18u / W'
+ sa=0 sb=0 sd=0 m=1
XM11 VI0 net4 Vdd Vdd pfet_03v3 L=0.5u W=80u nf=1 ad='int((nf+1)/2) * W/nf * 0.18u' as='int((nf+2)/2) * W/nf * 0.18u'
+ pd='2*int((nf+1)/2) * (W/nf + 0.18u)' ps='2*int((nf+2)/2) * (W/nf + 0.18u)' nrd='0.18u / W' nrs='0.18u / W'
+ sa=0 sb=0 sd=0 m=1
XM12 net4 net4 Vdd Vdd pfet_03v3 L=0.5u W=80u nf=1 ad='int((nf+1)/2) * W/nf * 0.18u' as='int((nf+2)/2) * W/nf * 0.18u'
+ pd='2*int((nf+1)/2) * (W/nf + 0.18u)' ps='2*int((nf+2)/2) * (W/nf + 0.18u)' nrd='0.18u / W' nrs='0.18u / W'
+ sa=0 sb=0 sd=0 m=1
XM9 VI2 net4 Vdd Vdd pfet_03v3 L=0.5u W=80u nf=1 ad='int((nf+1)/2) * W/nf * 0.18u' as='int((nf+2)/2) * W/nf * 0.18u'
+ pd='2*int((nf+1)/2) * (W/nf + 0.18u)' ps='2*int((nf+2)/2) * (W/nf + 0.18u)' nrd='0.18u / W' nrs='0.18u / W'
+ sa=0 sb=0 sd=0 m=1
XM10 net5 net5 Vdd Vdd pfet_03v3 L=0.5u W=40u nf=1 ad='int((nf+1)/2) * W/nf * 0.18u' as='int((nf+2)/2) * W/nf * 0.18u'
+ pd='2*int((nf+1)/2) * (W/nf + 0.18u)' ps='2*int((nf+2)/2) * (W/nf + 0.18u)' nrd='0.18u / W' nrs='0.18u / W'
+ sa=0 sb=0 sd=0 m=1
XM15 IB30Ref net5 Vdd Vdd pfet_03v3 L=0.5u W=40u nf=1 ad='int((nf+1)/2) * W/nf * 0.18u' as='int((nf+2)/2) * W/nf * 0.18u'
+ pd='2*int((nf+1)/2) * (W/nf + 0.18u)' ps='2*int((nf+2)/2) * (W/nf + 0.18u)' nrd='0.18u / W' nrs='0.18u / W'
+ sa=0 sb=0 sd=0 m=1
XM17 IB30Ref IB30Ref 0 0 nfet_03v3 L=0.5u W=40u nf=1 ad='int((nf+1)/2) * W/nf * 0.18u' as='int((nf+2)/2) * W/nf * 0.18u'
+ pd='2*int((nf+1)/2) * (W/nf + 0.18u)' ps='2*int((nf+2)/2) * (W/nf + 0.18u)' nrd='0.18u / W' nrs='0.18u / W'
+ sa=0 sb=0 sd=0 m=1
XM20 VI1a IB30Ref 0 0 nfet_03v3 L=0.5u W=40u nf=1 ad='int((nf+1)/2) * W/nf * 0.18u' as='int((nf+2)/2) * W/nf * 0.18u'
+ pd='2*int((nf+1)/2) * (W/nf + 0.18u)' ps='2*int((nf+2)/2) * (W/nf + 0.18u)' nrd='0.18u / W' nrs='0.18u / W'
+ sa=0 sb=0 sd=0 m=1
XM21 VI1b IB30Ref 0 0 nfet_03v3 L=0.5u W=40u nf=1 ad='int((nf+1)/2) * W/nf * 0.18u' as='int((nf+2)/2) * W/nf * 0.18u'
+ pd='2*int((nf+1)/2) * (W/nf + 0.18u)' ps='2*int((nf+2)/2) * (W/nf + 0.18u)' nrd='0.18u / W' nrs='0.18u / W'
+ sa=0 sb=0 sd=0 m=2
XM13 net4 IB30Ref 0 0 nfet_03v3 L=0.5u W=40u nf=1 ad='int((nf+1)/2) * W/nf * 0.18u' as='int((nf+2)/2) * W/nf * 0.18u'
+ pd='2*int((nf+1)/2) * (W/nf + 0.18u)' ps='2*int((nf+2)/2) * (W/nf + 0.18u)' nrd='0.18u / W' nrs='0.18u / W'
+ sa=0 sb=0 sd=0 m=2
XM30 net3 IB10 0 0 nfet_03v3 L=1u W=8u nf=1 ad='int((nf+1)/2) * W/nf * 0.18u' as='int((nf+2)/2) * W/nf * 0.18u'
+ pd='2*int((nf+1)/2) * (W/nf + 0.18u)' ps='2*int((nf+2)/2) * (W/nf + 0.18u)' nrd='0.18u / W' nrs='0.18u / W'
+ sa=0 sb=0 sd=0 m=2
XM14 net5 IB10 0 0 nfet_03v3 L=1u W=8u nf=1 ad='int((nf+1)/2) * W/nf * 0.18u' as='int((nf+2)/2) * W/nf * 0.18u'
+ pd='2*int((nf+1)/2) * (W/nf + 0.18u)' ps='2*int((nf+2)/2) * (W/nf + 0.18u)' nrd='0.18u / W' nrs='0.18u / W'
+ sa=0 sb=0 sd=0 m=3
.ends


* expanding   symbol:  common/cmos_buf.sym # of pins=3
** sym_path: blocks/dac/common/cmos_buf.sym
** sch_path: blocks/dac/common/cmos_buf.sch
.subckt cmos_buf ViBB Vi Vdd
*.ipin Vi
*.opin ViBB
*.ipin Vdd
XM49 ViB Vi 0 0 nfet_03v3 L=0.28u W=0.5u nf=1 ad='int((nf+1)/2) * W/nf * 0.18u' as='int((nf+2)/2) * W/nf * 0.18u'
+ pd='2*int((nf+1)/2) * (W/nf + 0.18u)' ps='2*int((nf+2)/2) * (W/nf + 0.18u)' nrd='0.18u / W' nrs='0.18u / W'
+ sa=0 sb=0 sd=0 m=1
XM50 ViB Vi Vdd Vdd pfet_03v3 L=0.28u W=1u nf=1 ad='int((nf+1)/2) * W/nf * 0.18u' as='int((nf+2)/2) * W/nf * 0.18u'
+ pd='2*int((nf+1)/2) * (W/nf + 0.18u)' ps='2*int((nf+2)/2) * (W/nf + 0.18u)' nrd='0.18u / W' nrs='0.18u / W'
+ sa=0 sb=0 sd=0 m=1
XM1 ViBB ViB 0 0 nfet_03v3 L=0.28u W=0.5u nf=1 ad='int((nf+1)/2) * W/nf * 0.18u' as='int((nf+2)/2) * W/nf * 0.18u'
+ pd='2*int((nf+1)/2) * (W/nf + 0.18u)' ps='2*int((nf+2)/2) * (W/nf + 0.18u)' nrd='0.18u / W' nrs='0.18u / W'
+ sa=0 sb=0 sd=0 m=1
XM2 ViBB ViB Vdd Vdd pfet_03v3 L=0.28u W=1u nf=1 ad='int((nf+1)/2) * W/nf * 0.18u' as='int((nf+2)/2) * W/nf * 0.18u'
+ pd='2*int((nf+1)/2) * (W/nf + 0.18u)' ps='2*int((nf+2)/2) * (W/nf + 0.18u)' nrd='0.18u / W' nrs='0.18u / W'
+ sa=0 sb=0 sd=0 m=1
.ends

.end
